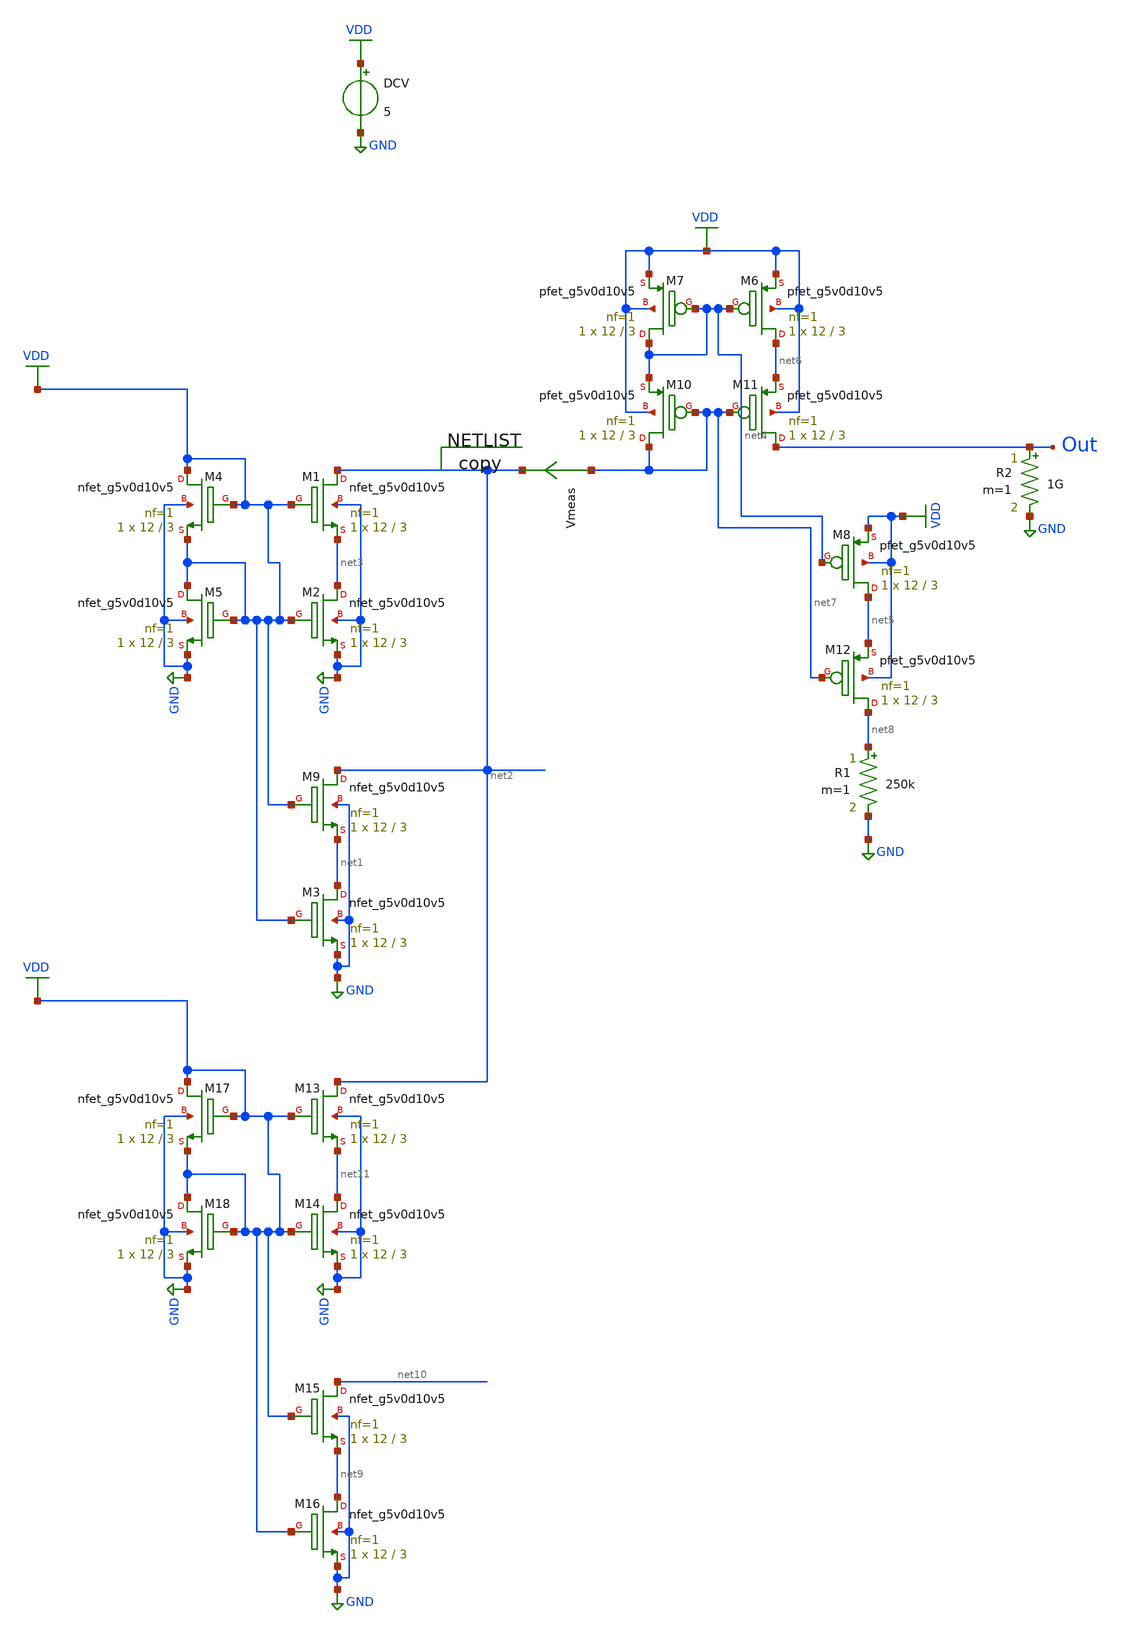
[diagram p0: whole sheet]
** sch_path: xschem/untitled-3.sch
**.subckt untitled-3
XM1 net2 VDD net3 GND sky130_fd_pr__nfet_g5v0d10v5 L=3 W=12 nf=1 ad='int((nf+1)/2) * W/nf * 0.29' as='int((nf+2)/2) * W/nf * 0.29'
+ pd='2*int((nf+1)/2) * (W/nf + 0.29)' ps='2*int((nf+2)/2) * (W/nf + 0.29)' nrd='0.29 / W' nrs='0.29 / W'
+ sa=0 sb=0 sd=0 mult=1 m=1
XM2 net3 VDD GND GND sky130_fd_pr__nfet_g5v0d10v5 L=3 W=12 nf=1 ad='int((nf+1)/2) * W/nf * 0.29' as='int((nf+2)/2) * W/nf * 0.29'
+ pd='2*int((nf+1)/2) * (W/nf + 0.29)' ps='2*int((nf+2)/2) * (W/nf + 0.29)' nrd='0.29 / W' nrs='0.29 / W'
+ sa=0 sb=0 sd=0 mult=1 m=1
XM9 net2 VDD net1 GND sky130_fd_pr__nfet_g5v0d10v5 L=3 W=12 nf=1 ad='int((nf+1)/2) * W/nf * 0.29' as='int((nf+2)/2) * W/nf * 0.29'
+ pd='2*int((nf+1)/2) * (W/nf + 0.29)' ps='2*int((nf+2)/2) * (W/nf + 0.29)' nrd='0.29 / W' nrs='0.29 / W'
+ sa=0 sb=0 sd=0 mult=1 m=1
XM3 net1 VDD GND GND sky130_fd_pr__nfet_g5v0d10v5 L=3 W=12 nf=1 ad='int((nf+1)/2) * W/nf * 0.29' as='int((nf+2)/2) * W/nf * 0.29'
+ pd='2*int((nf+1)/2) * (W/nf + 0.29)' ps='2*int((nf+2)/2) * (W/nf + 0.29)' nrd='0.29 / W' nrs='0.29 / W'
+ sa=0 sb=0 sd=0 mult=1 m=1
XM4 VDD VDD VDD GND sky130_fd_pr__nfet_g5v0d10v5 L=3 W=12 nf=1 ad='int((nf+1)/2) * W/nf * 0.29' as='int((nf+2)/2) * W/nf * 0.29'
+ pd='2*int((nf+1)/2) * (W/nf + 0.29)' ps='2*int((nf+2)/2) * (W/nf + 0.29)' nrd='0.29 / W' nrs='0.29 / W'
+ sa=0 sb=0 sd=0 mult=1 m=1
XM5 VDD VDD GND GND sky130_fd_pr__nfet_g5v0d10v5 L=3 W=12 nf=1 ad='int((nf+1)/2) * W/nf * 0.29' as='int((nf+2)/2) * W/nf * 0.29'
+ pd='2*int((nf+1)/2) * (W/nf + 0.29)' ps='2*int((nf+2)/2) * (W/nf + 0.29)' nrd='0.29 / W' nrs='0.29 / W'
+ sa=0 sb=0 sd=0 mult=1 m=1
XM6 net6 net4 VDD VDD sky130_fd_pr__pfet_g5v0d10v5 L=3 W=12 nf=1 ad='int((nf+1)/2) * W/nf * 0.29' as='int((nf+2)/2) * W/nf * 0.29'
+ pd='2*int((nf+1)/2) * (W/nf + 0.29)' ps='2*int((nf+2)/2) * (W/nf + 0.29)' nrd='0.29 / W' nrs='0.29 / W'
+ sa=0 sb=0 sd=0 mult=1 m=1
XM7 net4 net4 VDD VDD sky130_fd_pr__pfet_g5v0d10v5 L=3 W=12 nf=1 ad='int((nf+1)/2) * W/nf * 0.29' as='int((nf+2)/2) * W/nf * 0.29'
+ pd='2*int((nf+1)/2) * (W/nf + 0.29)' ps='2*int((nf+2)/2) * (W/nf + 0.29)' nrd='0.29 / W' nrs='0.29 / W'
+ sa=0 sb=0 sd=0 mult=1 m=1
XM8 net5 net4 VDD VDD sky130_fd_pr__pfet_g5v0d10v5 L=3 W=12 nf=1 ad='int((nf+1)/2) * W/nf * 0.29' as='int((nf+2)/2) * W/nf * 0.29'
+ pd='2*int((nf+1)/2) * (W/nf + 0.29)' ps='2*int((nf+2)/2) * (W/nf + 0.29)' nrd='0.29 / W' nrs='0.29 / W'
+ sa=0 sb=0 sd=0 mult=1 m=1
XM10 net7 net7 net4 VDD sky130_fd_pr__pfet_g5v0d10v5 L=3 W=12 nf=1 ad='int((nf+1)/2) * W/nf * 0.29' as='int((nf+2)/2) * W/nf * 0.29'
+ pd='2*int((nf+1)/2) * (W/nf + 0.29)' ps='2*int((nf+2)/2) * (W/nf + 0.29)' nrd='0.29 / W' nrs='0.29 / W'
+ sa=0 sb=0 sd=0 mult=1 m=1
XM11 Out net7 net6 VDD sky130_fd_pr__pfet_g5v0d10v5 L=3 W=12 nf=1 ad='int((nf+1)/2) * W/nf * 0.29' as='int((nf+2)/2) * W/nf * 0.29'
+ pd='2*int((nf+1)/2) * (W/nf + 0.29)' ps='2*int((nf+2)/2) * (W/nf + 0.29)' nrd='0.29 / W' nrs='0.29 / W'
+ sa=0 sb=0 sd=0 mult=1 m=1
XM12 net8 net7 net5 VDD sky130_fd_pr__pfet_g5v0d10v5 L=3 W=12 nf=1 ad='int((nf+1)/2) * W/nf * 0.29' as='int((nf+2)/2) * W/nf * 0.29'
+ pd='2*int((nf+1)/2) * (W/nf + 0.29)' ps='2*int((nf+2)/2) * (W/nf + 0.29)' nrd='0.29 / W' nrs='0.29 / W'
+ sa=0 sb=0 sd=0 mult=1 m=1
R1 net8 GND 250k m=1
DCV VDD GND 5
R2 Out GND 1G m=1
Vmeas net7 net2 0
.save i(vmeas)
XM13 net2 VDD net11 GND sky130_fd_pr__nfet_g5v0d10v5 L=3 W=12 nf=1 ad='int((nf+1)/2) * W/nf * 0.29' as='int((nf+2)/2) * W/nf * 0.29'
+ pd='2*int((nf+1)/2) * (W/nf + 0.29)' ps='2*int((nf+2)/2) * (W/nf + 0.29)' nrd='0.29 / W' nrs='0.29 / W'
+ sa=0 sb=0 sd=0 mult=1 m=1
XM14 net11 VDD GND GND sky130_fd_pr__nfet_g5v0d10v5 L=3 W=12 nf=1 ad='int((nf+1)/2) * W/nf * 0.29' as='int((nf+2)/2) * W/nf * 0.29'
+ pd='2*int((nf+1)/2) * (W/nf + 0.29)' ps='2*int((nf+2)/2) * (W/nf + 0.29)' nrd='0.29 / W' nrs='0.29 / W'
+ sa=0 sb=0 sd=0 mult=1 m=1
XM15 net10 VDD net9 GND sky130_fd_pr__nfet_g5v0d10v5 L=3 W=12 nf=1 ad='int((nf+1)/2) * W/nf * 0.29' as='int((nf+2)/2) * W/nf * 0.29'
+ pd='2*int((nf+1)/2) * (W/nf + 0.29)' ps='2*int((nf+2)/2) * (W/nf + 0.29)' nrd='0.29 / W' nrs='0.29 / W'
+ sa=0 sb=0 sd=0 mult=1 m=1
XM16 net9 VDD GND GND sky130_fd_pr__nfet_g5v0d10v5 L=3 W=12 nf=1 ad='int((nf+1)/2) * W/nf * 0.29' as='int((nf+2)/2) * W/nf * 0.29'
+ pd='2*int((nf+1)/2) * (W/nf + 0.29)' ps='2*int((nf+2)/2) * (W/nf + 0.29)' nrd='0.29 / W' nrs='0.29 / W'
+ sa=0 sb=0 sd=0 mult=1 m=1
XM17 VDD VDD VDD GND sky130_fd_pr__nfet_g5v0d10v5 L=3 W=12 nf=1 ad='int((nf+1)/2) * W/nf * 0.29' as='int((nf+2)/2) * W/nf * 0.29'
+ pd='2*int((nf+1)/2) * (W/nf + 0.29)' ps='2*int((nf+2)/2) * (W/nf + 0.29)' nrd='0.29 / W' nrs='0.29 / W'
+ sa=0 sb=0 sd=0 mult=1 m=1
XM18 VDD VDD GND GND sky130_fd_pr__nfet_g5v0d10v5 L=3 W=12 nf=1 ad='int((nf+1)/2) * W/nf * 0.29' as='int((nf+2)/2) * W/nf * 0.29'
+ pd='2*int((nf+1)/2) * (W/nf + 0.29)' ps='2*int((nf+2)/2) * (W/nf + 0.29)' nrd='0.29 / W' nrs='0.29 / W'
+ sa=0 sb=0 sd=0 mult=1 m=1
**** begin user architecture code

copy


** opencircuitdesign pdks install
.lib $::SKYWATER_MODELS/sky130.lib.spice tt



* this option enables mos model bin
* selection based on W/NF instead of W
.control
op
print all
save all
.endc


**** end user architecture code
**.ends
.GLOBAL GND
.GLOBAL VDD
.end
